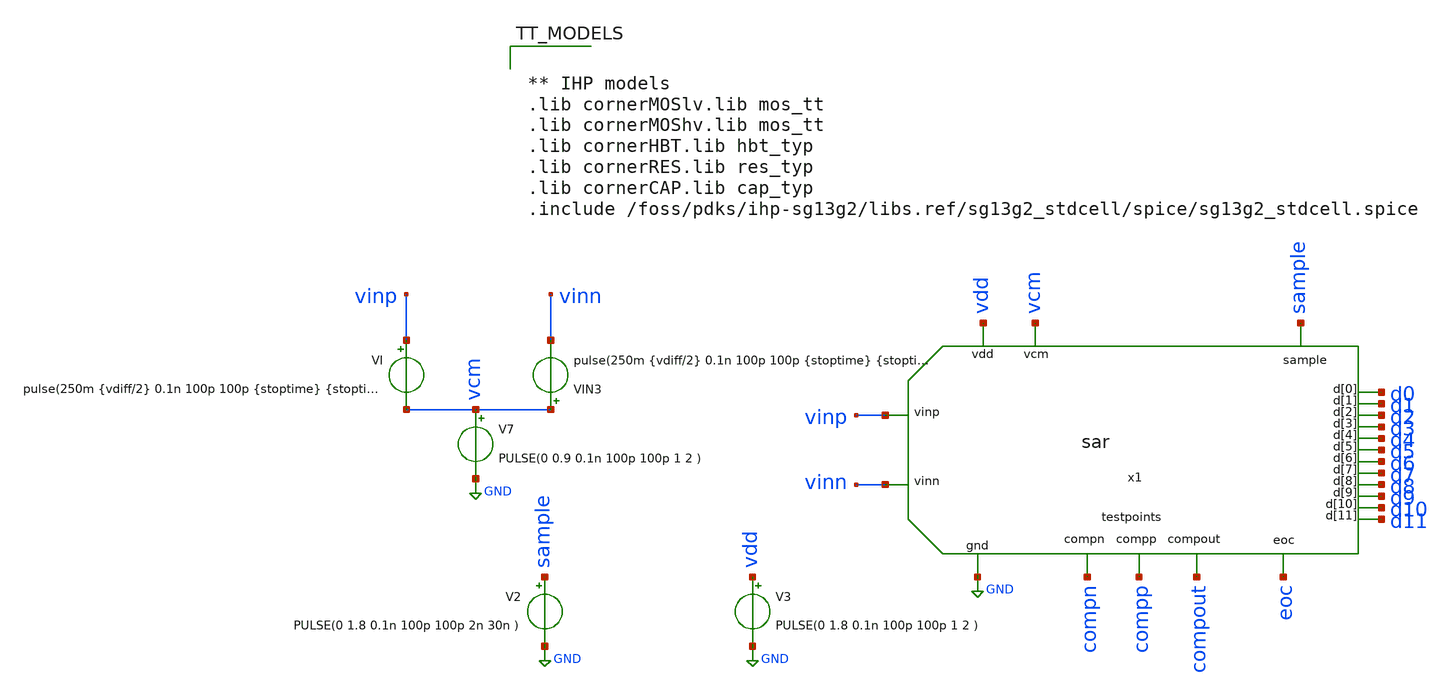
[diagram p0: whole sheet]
** sch_path: xschem/SAR_ADC/testbench/tb_sar_adc_template.sch
**.subckt tb_sar_adc_template
x1 vinp sample vinn GND vdd compn compp compout eoc d9 d7 d0 d11 d3 d4 d2 d1 d8 d6 d5 d10 vcm sar
VI vinp vcm pulse(250m {vdiff/2} 0.1n 100p 100p {stoptime} {stoptime+1} 1)
VIN3 vcm vinn pulse(250m {vdiff/2} 0.1n 100p 100p {stoptime} {stoptime+1} 1)
V2 sample GND PULSE(0 1.8 0.1n 100p 100p 2n 30n )
V3 vdd GND PULSE(0 1.8 0.1n 100p 100p 1 2 )
V7 vcm GND PULSE(0 0.9 0.1n 100p 100p 1 2 )
**** begin user architecture code


.param periodclk=1n
.param periodconv=20n
.param stoptime=1*periodconv
.param ro = 300
.param W_P = 1.0u
.param L_P = 0.13u
.param W_N = 1.0u
.param L_N = 0.13u
.param vdiff = 1
.options klu method=gear reltol=1e-2 abstol=1e-15 gmin=1e-15
.control
set lsb=878u
alterparam vdiff={&n * &lsb}
reset
tran 5p 20n
meas tran bit11 FIND d11 when eoc=1.7 CROSS=LAST
meas tran bit10 FIND d10 when eoc=1.7 CROSS=LAST
meas tran bit9 FIND d9 when eoc=1.7 CROSS=LAST
meas tran bit8 FIND d8 when eoc=1.7 CROSS=LAST
meas tran bit7 FIND d7 when eoc=1.7 CROSS=LAST
meas tran bit6 FIND d6 when eoc=1.7 CROSS=LAST
meas tran bit5 FIND d5 when eoc=1.7 CROSS=LAST
meas tran bit4 FIND d4 when eoc=1.7 CROSS=LAST
meas tran bit3 FIND d3 when eoc=1.7 CROSS=LAST
meas tran bit2 FIND d2 when eoc=1.7 CROSS=LAST
meas tran bit1 FIND d1 when eoc=1.7 CROSS=LAST
meas tran bit0 FIND d0 when eoc=1.7 CROSS=LAST
print bit11 bit10 bit9 bit8 bit7 bit6 bit5 bit4 bit3 bit2 bit1 bit0
print bit11 bit10 bit9 bit8 bit7 bit6 bit5 bit4 bit3 bit2 bit1 bit0 > ./../../out/sim{$n}.txt


*plot compp compn {compout + 4}
*plot {d0} {d1 + 4} {d2 + 8} {d3 + 12} {d4 + 16} {d5 + 20} {d6 + 24} {d7 + 28} {d8 + 32} {d9 + 36} {d10 + 40}
*+ {d11 + 44} {x1.comp_clk + 50} {compout + 55} {eoc + 60}  {compp - compn - 2}
*plot compp-compn x1.comp_clk compout
*plot sample eoc x1.x3.start
*plot {(((V(d11)/1.8)*2048 + (V(d10)/1.8)*1024 + (V(d9)/1.8)*512 + (V(d8)/1.8)*256 + (V(d7)/1.8)*128 + (V(d6)/1.8)*64 + (V(d5)/1.8)*32 + (V(d4)/1.8)*16 + (V(d3)/1.8)*8 + (V(d2)/1.8)*4 + (V(d1)/1.8)*2 + (V(d0)/1.8)) - 2048) * 1.8/2048}
*+ sample eoc vinp-vinn
*plot {((((0-V(d11))/1.8)*2048 + (V(d10)/1.8)*1024 + (V(d9)/1.8)*512 + (V(d8)/1.8)*256 + (V(d7)/1.8)*128 + (V(d6)/1.8)*64 + (V(d5)/1.8)*32 + (V(d4)/1.8)*16 + (V(d3)/1.8)*8 + (V(d2)/1.8)*4 + (V(d1)/1.8)*2 + (V(d0)/1.8)) + 2048)*1.8/2048}
*+ sample eoc vinp-vinn
*wrdata adc_signals.csv time V(d0) V(d1) V(d2) V(d3) V(d4) V(d5) V(d6) V(d7) V(d8) V(d9) V(d10)
*+ V(d11) vinp vinn eoc sample compout compp compn x1.comp_clk
*write adc_signals.raw time V(d0) V(d1) V(d2) V(d3) V(d4) V(d5) V(d6) V(d7) V(d8) V(d9) V(d10)
*+ V(d11) vinp vinn eoc sample compout compp compn x1.comp_clk
*quit
.endc




** IHP models
.lib cornerMOSlv.lib mos_tt
.lib cornerMOShv.lib mos_tt
.lib cornerHBT.lib hbt_typ
.lib cornerRES.lib res_typ
.lib cornerCAP.lib cap_typ
.include /foss/pdks/ihp-sg13g2/libs.ref/sg13g2_stdcell/spice/sg13g2_stdcell.spice


**** end user architecture code
**.ends
.GLOBAL GND
.end
